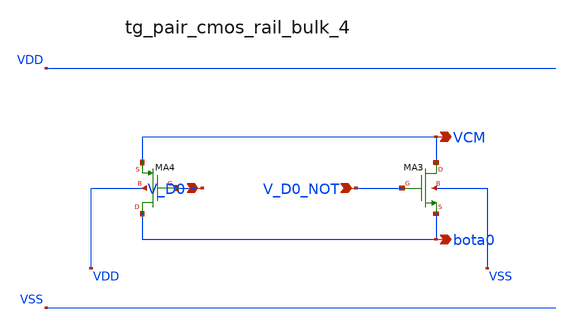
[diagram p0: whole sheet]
** sch_path: analog-db/raw/ia_005_hsu_pga_ideal/hier/blocks/tg_pair_cmos_rail_bulk_4.sch
**.subckt tg_pair_cmos_rail_bulk_4 V_D0 V_D0_NOT VCM bota0
*.ipin V_D0
*.ipin V_D0_NOT
*.opin VCM
*.opin bota0
XMA3 VCM V_D0_NOT bota0 VSS sg13_lv_nmos w=x_dut_xma3_w l=x_dut_xma3_l ng=1 m=x_dut_xma3_m
XMA4 bota0 V_D0 VCM VDD sg13_lv_pmos w=x_dut_xma4_w l=x_dut_xma4_l ng=1 m=x_dut_xma4_m
**.ends
.end
